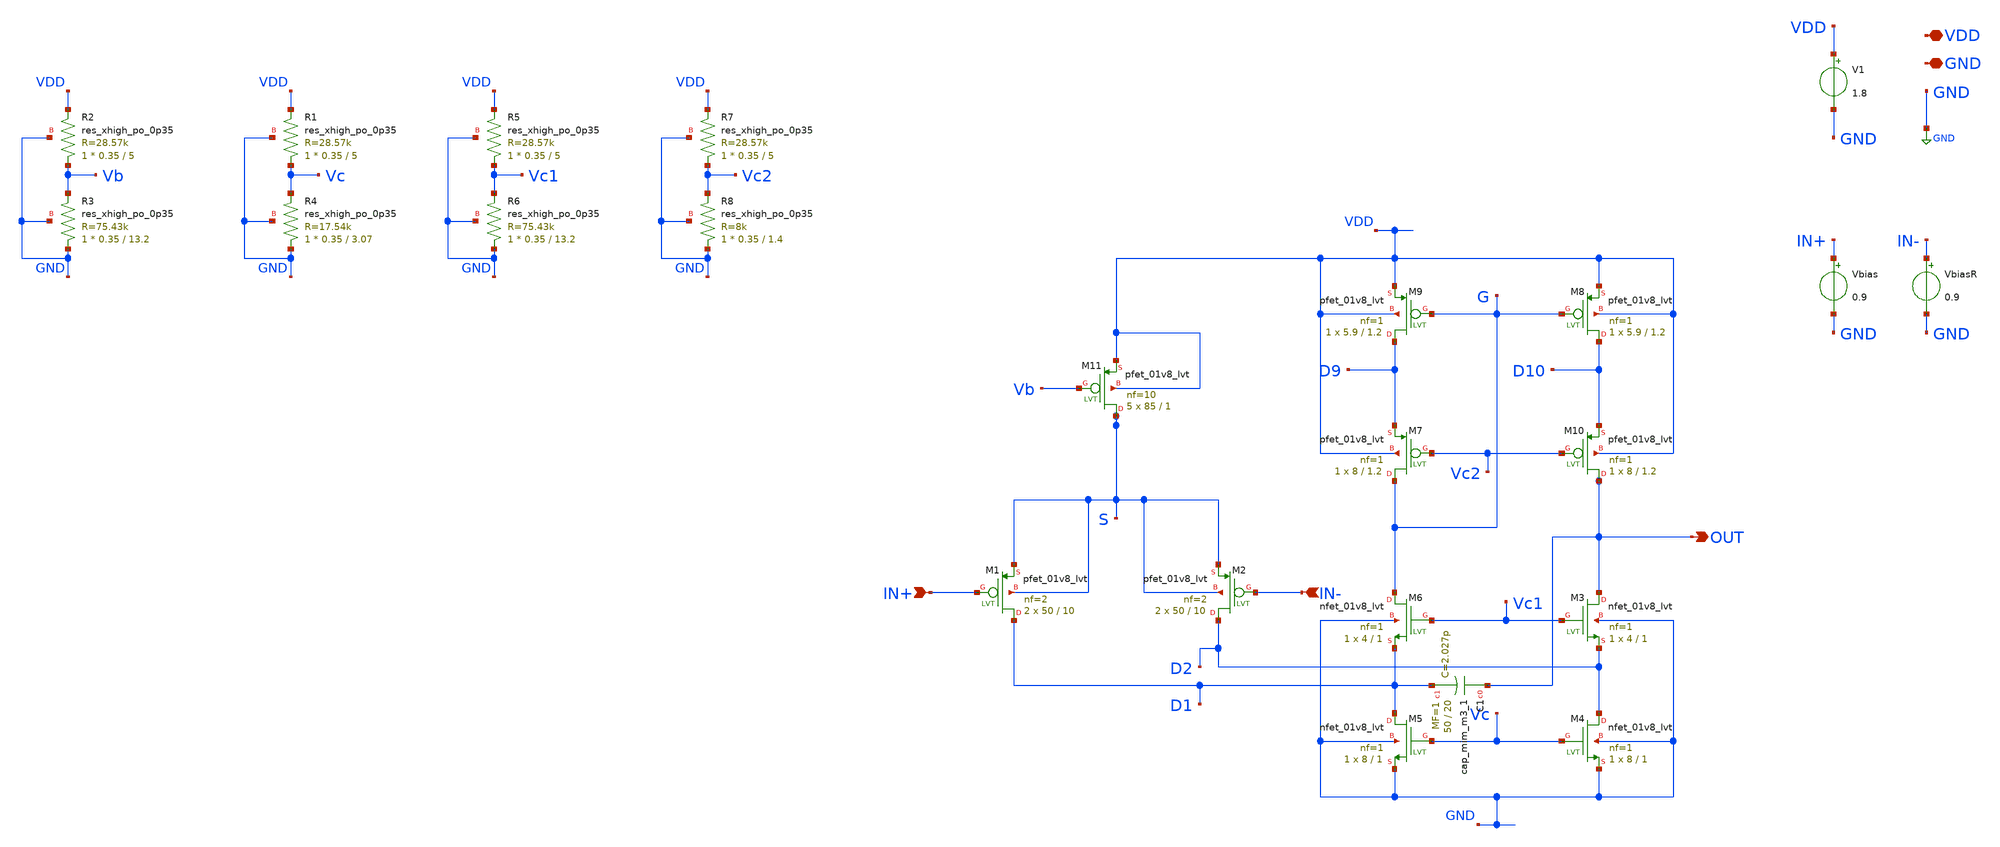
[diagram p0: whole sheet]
** sch_path: xschem/OTA_FoldedCascode1_1.sch
**.subckt OTA_FoldedCascode1_1 VDD GND IN+ IN- OUT
*.iopin VDD
*.iopin GND
*.ipin IN+
*.ipin IN-
*.opin OUT
V1 VDD GND 1.8
Vbias IN+ GND 0.9
VbiasR IN- GND 0.9
XM11 S Vb VDD VDD sky130_fd_pr__pfet_01v8_lvt L=1 W=85 nf=10 ad='int((nf+1)/2) * W/nf * 0.29' as='int((nf+2)/2) * W/nf * 0.29'
+ pd='2*int((nf+1)/2) * (W/nf + 0.29)' ps='2*int((nf+2)/2) * (W/nf + 0.29)' nrd='0.29 / W' nrs='0.29 / W'
+ sa=0 sb=0 sd=0 mult=5 m=5
XM1 D1 IN+ S S sky130_fd_pr__pfet_01v8_lvt L=10 W=50 nf=2 ad='int((nf+1)/2) * W/nf * 0.29' as='int((nf+2)/2) * W/nf * 0.29'
+ pd='2*int((nf+1)/2) * (W/nf + 0.29)' ps='2*int((nf+2)/2) * (W/nf + 0.29)' nrd='0.29 / W' nrs='0.29 / W'
+ sa=0 sb=0 sd=0 mult=2 m=2
XM2 D2 IN- S S sky130_fd_pr__pfet_01v8_lvt L=10 W=50 nf=2 ad='int((nf+1)/2) * W/nf * 0.29' as='int((nf+2)/2) * W/nf * 0.29'
+ pd='2*int((nf+1)/2) * (W/nf + 0.29)' ps='2*int((nf+2)/2) * (W/nf + 0.29)' nrd='0.29 / W' nrs='0.29 / W'
+ sa=0 sb=0 sd=0 mult=2 m=2
XM3 OUT Vc1 D2 GND sky130_fd_pr__nfet_01v8_lvt L=1 W=4 nf=1 ad='int((nf+1)/2) * W/nf * 0.29' as='int((nf+2)/2) * W/nf * 0.29'
+ pd='2*int((nf+1)/2) * (W/nf + 0.29)' ps='2*int((nf+2)/2) * (W/nf + 0.29)' nrd='0.29 / W' nrs='0.29 / W'
+ sa=0 sb=0 sd=0 mult=1 m=1
XM4 D2 Vc GND GND sky130_fd_pr__nfet_01v8_lvt L=1 W=8 nf=1 ad='int((nf+1)/2) * W/nf * 0.29' as='int((nf+2)/2) * W/nf * 0.29'
+ pd='2*int((nf+1)/2) * (W/nf + 0.29)' ps='2*int((nf+2)/2) * (W/nf + 0.29)' nrd='0.29 / W' nrs='0.29 / W'
+ sa=0 sb=0 sd=0 mult=1 m=1
XM5 D1 Vc GND GND sky130_fd_pr__nfet_01v8_lvt L=1 W=8 nf=1 ad='int((nf+1)/2) * W/nf * 0.29' as='int((nf+2)/2) * W/nf * 0.29'
+ pd='2*int((nf+1)/2) * (W/nf + 0.29)' ps='2*int((nf+2)/2) * (W/nf + 0.29)' nrd='0.29 / W' nrs='0.29 / W'
+ sa=0 sb=0 sd=0 mult=1 m=1
XM6 G Vc1 D1 GND sky130_fd_pr__nfet_01v8_lvt L=1 W=4 nf=1 ad='int((nf+1)/2) * W/nf * 0.29' as='int((nf+2)/2) * W/nf * 0.29'
+ pd='2*int((nf+1)/2) * (W/nf + 0.29)' ps='2*int((nf+2)/2) * (W/nf + 0.29)' nrd='0.29 / W' nrs='0.29 / W'
+ sa=0 sb=0 sd=0 mult=1 m=1
XR2 Vb VDD GND sky130_fd_pr__res_xhigh_po_0p35 L=5 mult=1 m=1
XR3 GND Vb GND sky130_fd_pr__res_xhigh_po_0p35 L=13.2 mult=1 m=1
XR1 Vc VDD GND sky130_fd_pr__res_xhigh_po_0p35 L=5 mult=1 m=1
XR4 GND Vc GND sky130_fd_pr__res_xhigh_po_0p35 L=3.07 mult=1 m=1
XR5 Vc1 VDD GND sky130_fd_pr__res_xhigh_po_0p35 L=5 mult=1 m=1
XR6 GND Vc1 GND sky130_fd_pr__res_xhigh_po_0p35 L=13.2 mult=1 m=1
XR7 Vc2 VDD GND sky130_fd_pr__res_xhigh_po_0p35 L=5 mult=1 m=1
XR8 GND Vc2 GND sky130_fd_pr__res_xhigh_po_0p35 L=1.4 mult=1 m=1
XM7 G Vc2 D9 VDD sky130_fd_pr__pfet_01v8_lvt L=1.2 W=8 nf=1 ad='int((nf+1)/2) * W/nf * 0.29' as='int((nf+2)/2) * W/nf * 0.29'
+ pd='2*int((nf+1)/2) * (W/nf + 0.29)' ps='2*int((nf+2)/2) * (W/nf + 0.29)' nrd='0.29 / W' nrs='0.29 / W'
+ sa=0 sb=0 sd=0 mult=1 m=1
XM9 D9 G VDD VDD sky130_fd_pr__pfet_01v8_lvt L=1.2 W=5.9 nf=1 ad='int((nf+1)/2) * W/nf * 0.29' as='int((nf+2)/2) * W/nf * 0.29'
+ pd='2*int((nf+1)/2) * (W/nf + 0.29)' ps='2*int((nf+2)/2) * (W/nf + 0.29)' nrd='0.29 / W' nrs='0.29 / W'
+ sa=0 sb=0 sd=0 mult=1 m=1
XM8 D10 G VDD VDD sky130_fd_pr__pfet_01v8_lvt L=1.2 W=5.9 nf=1 ad='int((nf+1)/2) * W/nf * 0.29' as='int((nf+2)/2) * W/nf * 0.29'
+ pd='2*int((nf+1)/2) * (W/nf + 0.29)' ps='2*int((nf+2)/2) * (W/nf + 0.29)' nrd='0.29 / W' nrs='0.29 / W'
+ sa=0 sb=0 sd=0 mult=1 m=1
XM10 OUT Vc2 D10 VDD sky130_fd_pr__pfet_01v8_lvt L=1.2 W=8 nf=1 ad='int((nf+1)/2) * W/nf * 0.29' as='int((nf+2)/2) * W/nf * 0.29'
+ pd='2*int((nf+1)/2) * (W/nf + 0.29)' ps='2*int((nf+2)/2) * (W/nf + 0.29)' nrd='0.29 / W' nrs='0.29 / W'
+ sa=0 sb=0 sd=0 mult=1 m=1
XC1 OUT D1 sky130_fd_pr__cap_mim_m3_1 W=50 L=20 MF=1 m=1
**** begin user architecture code



* ngspice commands

.options savecurrents

.control
save all
save @m.xm1.msky130_fd_pr__pfet_01v8_lvt[gm]
save @m.xm2.msky130_fd_pr__pfet_01v8_lvt[gm]
save @m.xm3.msky130_fd_pr__nfet_01v8_lvt[gm]
save @m.xm4.msky130_fd_pr__nfet_01v8_lvt[gm]
save @m.xm5.msky130_fd_pr__nfet_01v8_lvt[gm]
save @m.xm6.msky130_fd_pr__nfet_01v8_lvt[gm]
save @m.xm7.msky130_fd_pr__pfet_01v8_lvt[gm]
save @m.xm8.msky130_fd_pr__pfet_01v8_lvt[gm]
save @m.xm9.msky130_fd_pr__pfet_01v8_lvt[gm]
save @m.xm10.msky130_fd_pr__pfet_01v8_lvt[gm]

   op
   remzerovec
   write OTA_FoldedCascode1_1.raw
   set appendwrite
   dc Vbias 0.899 0.901 0.00001
   *dc Vbias 0.899 0.901 0.0001
   *dc Vbias 0 1.8 0.01
   *remzerovec
   plot v(out),v(in+)
   plot deriv(v(out))

   write OTA_FoldedCascode1_1.raw

.endc
.end



.lib $::SKYWATER_MODELS/sky130.lib.spice tt
**** end user architecture code
**.ends
.GLOBAL GND
.end
